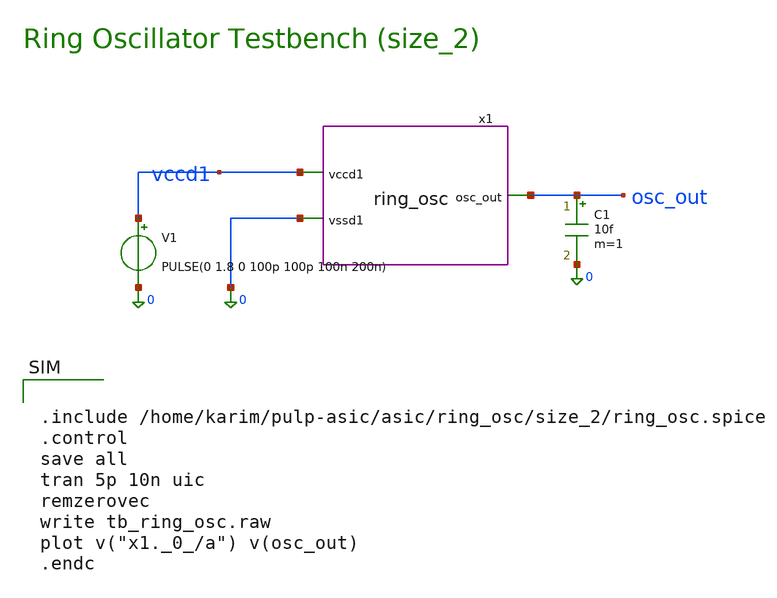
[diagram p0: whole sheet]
** sch_path: asic/ring_osc/size_2/tb_ring_osc.sch
**.subckt tb_ring_osc
x1 osc_out vccd1 0 ring_osc
V1 vccd1 0 PULSE(0 1.8 0 100p 100p 100n 200n)
C1 osc_out 0 10f m=1
**** begin user architecture code

.lib $::SKYWATER_MODELS/sky130.lib.spice tt



.include /home/karim/pulp-asic/asic/ring_osc/size_2/ring_osc.spice
.control
save all
tran 5p 10n uic
remzerovec
write tb_ring_osc.raw
plot v("x1._0_/a") v(osc_out)
.endc


**** end user architecture code
**.ends
.end
